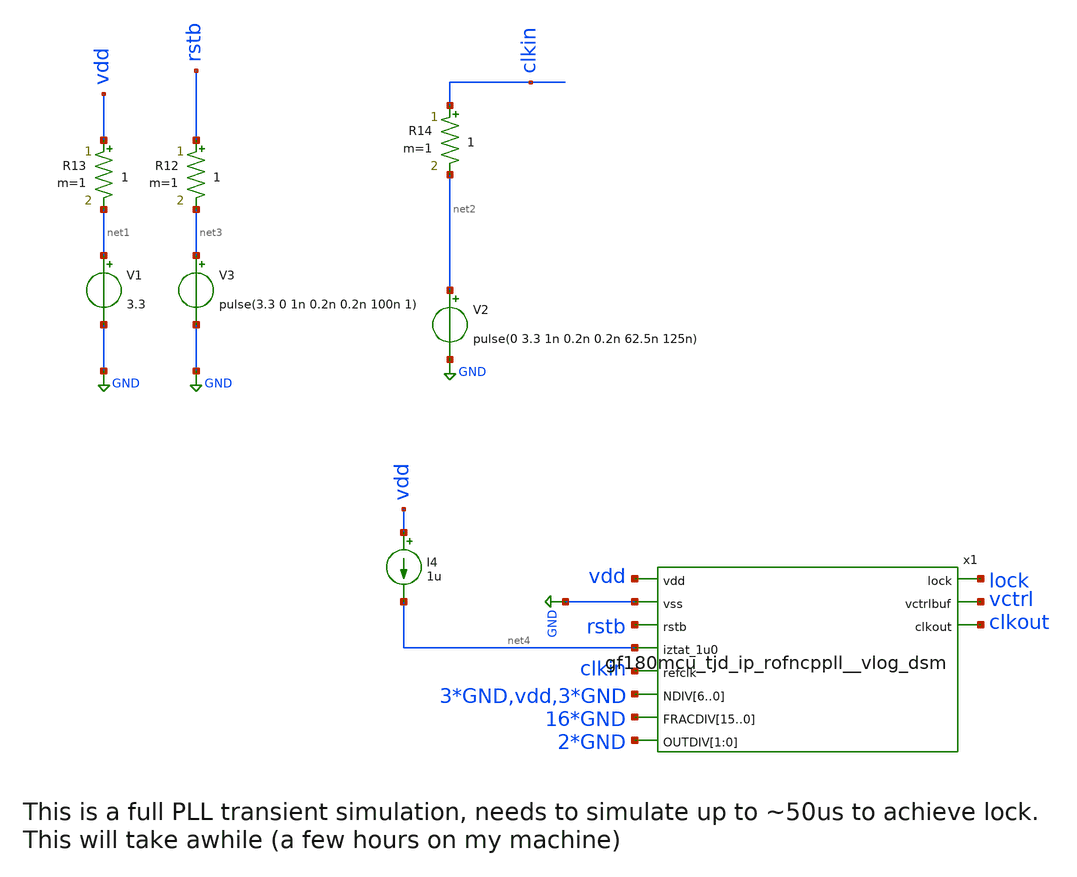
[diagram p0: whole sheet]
** sch_path: xschem/tb_pll_top__vlog.sch
**.subckt tb_pll_top__vlog
V1 net1 GND 3.3
V2 net2 GND pulse(0 3.3 1n 0.2n 0.2n 62.5n 125n)
V3 net3 GND pulse(3.3 0 1n 0.2n 0.2n 100n 1)
R12 rstb net3 1 m=1
R13 vdd net1 1 m=1
R14 clkin net2 1 m=1
I4 vdd net4 1u
x1 lock vdd GND rstb vctrl net4 clkout clkin GND GND GND vdd GND GND GND GND GND GND GND GND GND GND
+ GND GND GND GND GND GND GND GND GND GND GND gf180mcu_tjd_ip_rofncppll__vlog_dsm
**** begin user architecture code


.include /usr/local/share/pdk/gf180mcuD/libs.tech/ngspice/design.ngspice
.lib /usr/local/share/pdk/gf180mcuD/libs.tech/ngspice/sm141064.ngspice typical
.lib /usr/local/share/pdk/gf180mcuD/libs.tech/ngspice/sm141064.ngspice cap_mim
.lib /usr/local/share/pdk/gf180mcuD/libs.tech/ngspice/sm141064.ngspice mimcap_typical
.lib /usr/local/share/pdk/gf180mcuD/libs.tech/ngspice/sm141064.ngspice moscap_typical
.lib /usr/local/share/pdk/gf180mcuD/libs.tech/ngspice/sm141064.ngspice res_typical
.option temp=25
* .ic V(vctrl_unfilt)=0 V(vctrl)=0


.control
tran 12p 70u
run
plot i(V1)
plot v(clkin)
plot v(clkout)
plot v(xpll.vco)
plot v(xpll.clkfb)
plot v(vctrl)
plot v(xpll.up) v(xpll.dn)
* plot v(x2.vrep) v(x2.vbiasp) v(x2.vdummy) v(vctrl_unfilt)
plot lock

meas tran tper_ref TRIG v(clkin) VAL=1.65 RISE=50 TARG v(clkin) VAL=1.65 RISE=51
meas tran tper_out TRIG v(clkout) VAL=1.65 TD=49.9u RISE=1 TARG v(clkout) VAL=1.65 TD=49.9u RISE=2

let fref_mhz = 1 / tper_ref / 1e6
let fout_mhz = 1 / tper_out / 1e6

echo REFCLK = $&fref_mhz MHz
echo FOUT = $&fout_mhz MHz

meas tran tper_out TRIG v(clkout) VAL=1.65 TD=49.99u RISE=1 TARG v(clkout) VAL=1.65 TD=49.99u RISE=2
let fout_mhz = 1 / tper_out / 1e6
echo FOUT2 = $&fout_mhz MHz

meas tran t1 WHEN v(clkout)=1.65 RISE=1 TD=47u
meas tran t2 WHEN v(clkout)=1.65 RISE=501 TD=47u
let f0 = 500 / (t2-t1)
echo f0 = $&f0

.endc


**** end user architecture code
**.ends
.GLOBAL GND
.end
